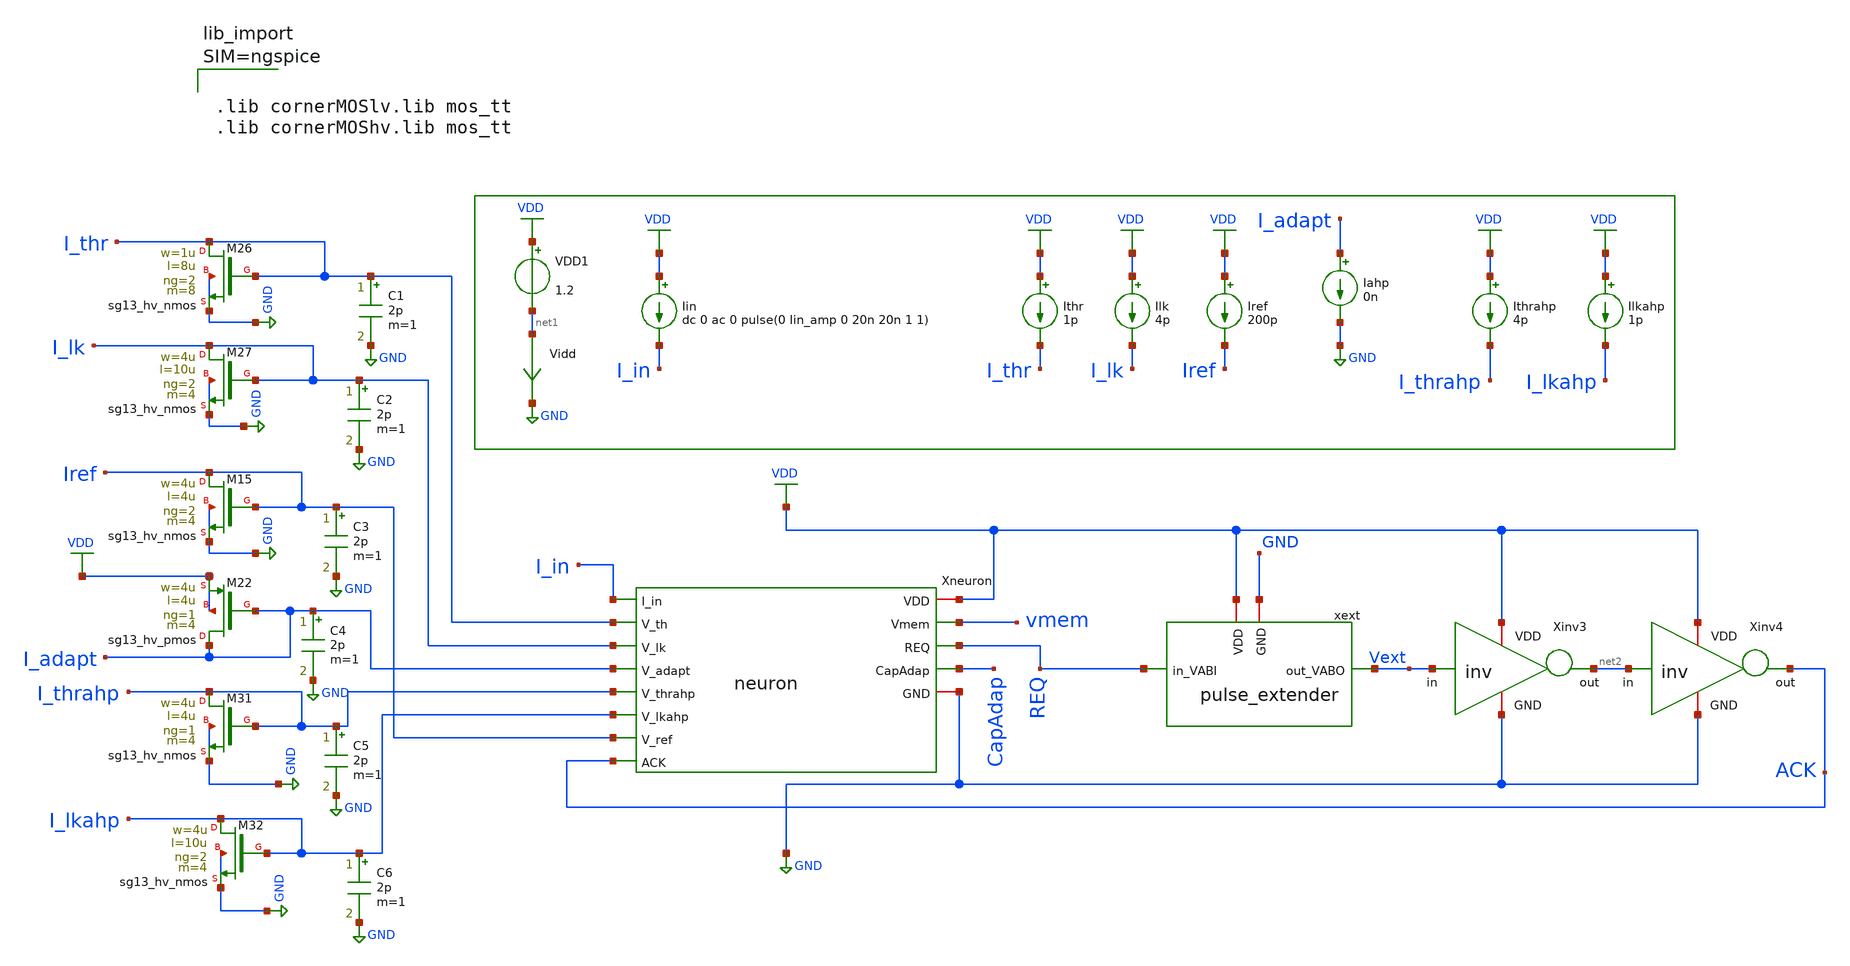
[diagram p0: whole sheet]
** sch_path: xschem/neuron_pulext_tb.sch
**.subckt neuron_pulext_tb
Xneuron VDD I_in I_thr I_lk vmem REQ I_adapt I_thrahp CapAdap ACK I_lkahp Iref GND neuron
Ithr VDD I_thr 1p
Ilk VDD I_lk 4p
Iahp I_adapt GND 0n
Iin VDD I_in dc 0 ac 0 pulse(0 Iin_amp 0 20n 20n 1 1)
VDD1 VDD net1 1.2
Iref VDD Iref 200p
Vidd net1 GND 0
.save i(vidd)
Ilkahp VDD I_lkahp 1p
Ithrahp VDD I_thrahp 4p
XM26 I_thr I_thr GND GND sg13_hv_nmos w=1u l=8u ng=2 m=8 mm_ok=1
XM27 I_lk I_lk GND GND sg13_hv_nmos w=4u l=10u ng=2 m=4 mm_ok=1
XM15 Iref Iref GND GND sg13_hv_nmos w=4u l=4u ng=2 m=4 mm_ok=1
XM22 I_adapt I_adapt VDD VDD sg13_hv_pmos w=4u l=4u ng=1 m=4 mm_ok=1
XM31 I_thrahp I_thrahp GND GND sg13_hv_nmos w=4u l=4u ng=1 m=4 mm_ok=1
XM32 I_lkahp I_lkahp GND GND sg13_hv_nmos w=4u l=10u ng=2 m=4 mm_ok=1
Xinv3 VDD Vext net2 GND inv
Xinv4 VDD net2 ACK GND inv
C1 I_thr GND 2p m=1
C2 I_lk GND 2p m=1
C3 Iref GND 2p m=1
C4 I_adapt GND 2p m=1
C5 I_thrahp GND 2p m=1
C6 I_lkahp GND 2p m=1
xext VDD GND Vext REQ pulse_extender
**** begin user architecture code



.param temp=27
.param Iin_amp=200p

.ic V(vmem)=0 V(xneuron.xref.vref)=0 V(REQ)=0 V(ACK)=0 V(CapAdap)=0

.options gmin=1e-13
.control



* ======================================================
*  Iin sweep - measure firing rate of V(REQ) vs Iin
* ======================================================
*  For each DC value of Iin a transient simulation is run.
*  Rising-edge crossings of V(REQ) through a threshold
*  are counted after a settling window and the firing
*  frequency is computed.  Results go to neuron_iin_sweep.raw
* ======================================================

* --- Sweep parameters (Amps) - edit as needed ---
let iin_start = 0
let iin_stop  = 4000e-12
let iin_step  = 200e-12

* --- Compute number of sweep points ---
let num_pts = (iin_stop - iin_start) / iin_step + 1

* --- Create a new plot to hold the accumulated results ---
setplot new
set resplot = $curplot
let iin_values   = unitvec(num_pts)
let firing_rates = unitvec(num_pts)
let sweep_idx = 0
set t_sim = 50m

* --- Main sweep loop ---
dowhile sweep_idx < num_pts

  * Compute cur_iin fresh each iteration to avoid float drift
  let cur_iin = iin_start + sweep_idx * iin_step

  echo
  echo ============================================
  echo   Sweep point: Iin = $&cur_iin A
  echo ============================================

  * Save cur_iin to a shell variable before tran changes the plot context
  set cur_iin_val = $&cur_iin

  * Set the Iin_amp parameter to the current sweep value.
  alterparam Iin_amp = $cur_iin_val
  reset

  save V(REQ)

  * Run transient analysis with adaptive time
  echo   t_sim = $t_sim
  tran 50n $t_sim

  * --- Measure firing frequency using meas tran ---
  * Skip 1st spike (startup glitch), use 2nd-4th spikes
  let t_rise2 = 0
  let t_rise3 = 0
  let t_rise4 = 0
  meas tran t_rise2 WHEN v(REQ)=0.6 RISE=2
  meas tran t_rise3 WHEN v(REQ)=0.6 RISE=3
  meas tran t_rise4 WHEN v(REQ)=0.6 RISE=4

  * Use best available data for frequency
  if t_rise4 > 0
    * 4+ spikes: use 3rd-4th ISI
    let f_rate = 1.0 / (t_rise4 - t_rise3)
  else
    if t_rise3 > 0
      * 3 spikes: use 2nd-3rd ISI
      let f_rate = 1.0 / (t_rise3 - t_rise2)
    else
      if t_rise2 > 0
        * 2 spikes: estimate rate from time to 2nd spike
        let f_rate = 1.0 / t_rise2
      else
        * No real spikes (only glitch or none)
        let f_rate = 0
      end
    end
  end

  echo   freq = $&f_rate Hz

  * --- Update t_sim for next sweep point ---
  * Need ~5 spikes worth of time, clamp to [1ms, 50ms]
  if f_rate > 0
    let t_next = 5.0 / f_rate
    if t_next < 1e-3
      let t_next = 1e-3
    end
    if t_next > 50e-3
      let t_next = 50e-3
    end
    set t_sim = $&t_next
  end

  * --- Store this point's results in the result plot ---
  set save_freq = $&f_rate
  setplot $resplot
  let iin_values[sweep_idx]   = $cur_iin_val
  let firing_rates[sweep_idx] = $save_freq
  let sweep_idx = sweep_idx + 1

end

* --- Write the result vectors to a .raw file ---
setplot $resplot
write neuron_iin_sweep.raw iin_values firing_rates

echo
echo ============================================
echo   Iin sweep complete!
echo   Results saved to:  neuron_iin_sweep.raw
echo   Vectors:
echo     iin_values   (A)  - input current
echo     firing_rates (Hz) - neuron firing rate
echo ============================================

.endc







.lib cornerMOSlv.lib mos_tt
.lib cornerMOShv.lib mos_tt


**** end user architecture code
**.ends
.GLOBAL GND
.GLOBAL VDD
.end
